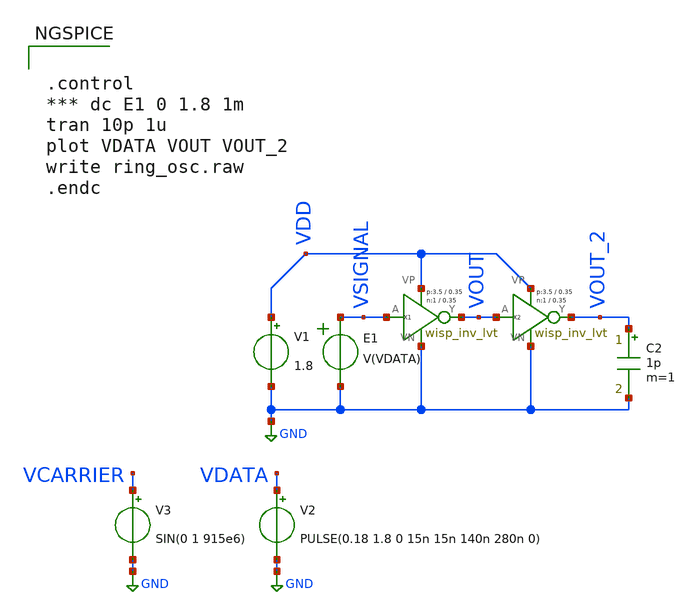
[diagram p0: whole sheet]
** sch_path: tb_wisp_inv_lvt.sch
**.subckt tb_wisp_inv_lvt
V1 VDD GND 1.8
X1 VSIGNAL VOUT VDD GND wisp_inv_lvt W_N=1 L_N=0.35 W_P=3.5 L_P=0.35 m=1
C2 VOUT_2 GND 1p m=1
E1 VSIGNAL GND VOL=' V(VDATA) '
V3 VCARRIER GND SIN(0 1 915e6)
V2 VDATA GND PULSE(0.18 1.8 0 15n 15n 140n 280n 0)
X2 VOUT VOUT_2 VDD GND wisp_inv_lvt W_N=1 L_N=0.35 W_P=3.5 L_P=0.35 m=1
**** begin user architecture code


.control
*** dc E1 0 1.8 1m
tran 10p 1u
plot VDATA VOUT VOUT_2
write ring_osc.raw
.endc


 .lib $::SKYWATER_MODELS/sky130.lib.spice tt

.param mc_mm_switch=0
.param mc_pr_switch=1


**** end user architecture code
**.ends

* expanding   symbol:  HPLP-UHF-RFID-SKY130/wisp_inv_lvt.sym # of pins=4
** sym_path: wisp_inv_lvt.sym
** sch_path: wisp_inv_lvt.sch
.subckt wisp_inv_lvt A Y VP VN    W_N=1 L_N=0.35 W_P=3.5 L_P=0.35
*.ipin A
*.opin Y
*.iopin VN
*.iopin VP
XM1 Y A VN VN sky130_fd_pr__nfet_01v8_lvt L=L_N W=W_N nf=1 ad='int((1 + 1)/2) * W_N / 1 * 0.29' as='int((1 + 2)/2) * W_N / 1 * 0.29'
+ pd='2*int((1 + 1)/2) * (W_N / 1 + 0.29)' ps='2*int((1 + 2)/2) * (W_N / 1 + 0.29)' nrd='0.29 / W_N ' nrs='0.29 / W_N '
+ sa=0 sb=0 sd=0 mult=1 m=1
XM2 Y A VP VP sky130_fd_pr__pfet_01v8_lvt L=L_P W=W_P nf=1 ad='int((1 + 1)/2) * W_P / 1 * 0.29' as='int((1 + 2)/2) * W_P / 1 * 0.29'
+ pd='2*int((1 + 1)/2) * (W_P / 1 + 0.29)' ps='2*int((1 + 2)/2) * (W_P / 1 + 0.29)' nrd='0.29 / W_P ' nrs='0.29 / W_P '
+ sa=0 sb=0 sd=0 mult=1 m=1
.ends

.GLOBAL GND
.end
